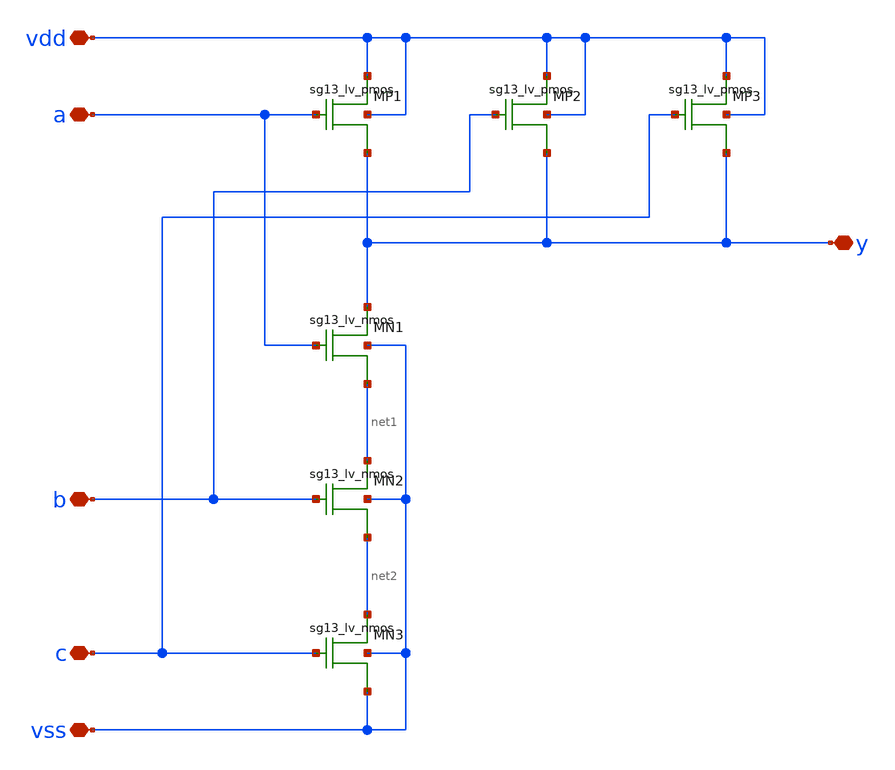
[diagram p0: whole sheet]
** sch_path: xschem/logic_gates/NAND3LV.sch
**.subckt NAND3LV vdd vss y a b c
*.iopin vdd
*.iopin vss
*.iopin y
*.iopin a
*.iopin b
*.iopin c
XMP1 vdd a y vdd sg13_lv_pmos w=1.0u l=0.13u ng=1 m=1
XMP2 vdd b y vdd sg13_lv_pmos w=1.0u l=0.13u ng=1 m=1
XMP3 vdd c y vdd sg13_lv_pmos w=1.0u l=0.13u ng=1 m=1
XMN1 y a net1 vss sg13_lv_nmos w=1.2u l=0.13u ng=1 m=1
XMN2 net1 b net2 vss sg13_lv_nmos w=1.2u l=0.13u ng=1 m=1
XMN3 net2 c vss vss sg13_lv_nmos w=1.2u l=0.13u ng=1 m=1
**.ends
.end
